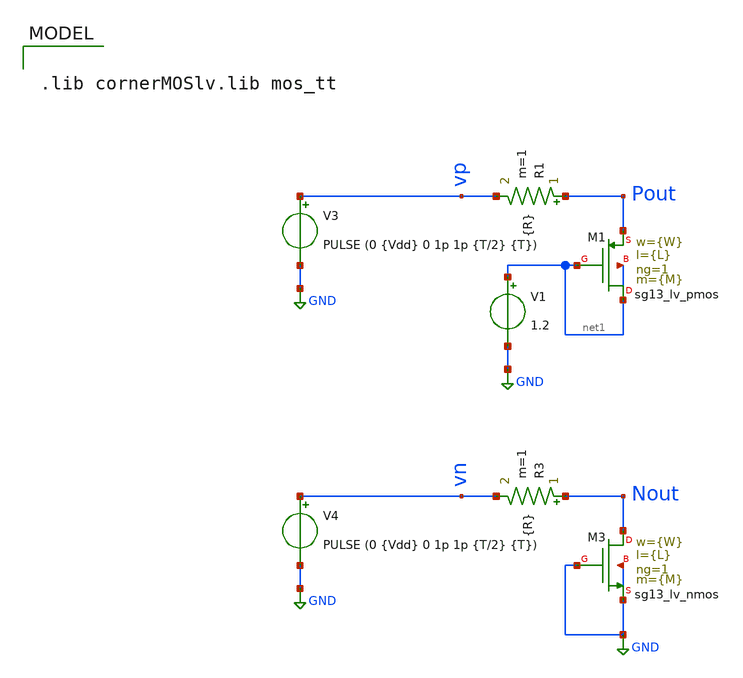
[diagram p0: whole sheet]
** sch_path: xschem/TB/TB_lvmos_Cdrain.sch
**.subckt TB_lvmos_Cdrain
R1 Pout vp {R} m=1
V3 vp GND PULSE (0 {Vdd} 0 1p 1p {T/2} {T})
V1 net1 GND 1.2
R3 Nout vn {R} m=1
V4 vn GND PULSE (0 {Vdd} 0 1p 1p {T/2} {T})
XM3 Nout GND GND GND sg13_lv_nmos w={W} l={L} ng=1 m={M} mm_ok=1
XM1 net1 net1 Pout net1 sg13_lv_pmos w={W} l={L} ng=1 m={M} mm_ok=1
**** begin user architecture code

.lib cornerMOSlv.lib mos_tt



.param R = 100k
.parameter T = 10n
.param Vdd = 1.8

.ic v(Pout) = 0
.ic v(Nout) = 0

* MOS Param
.param temp=27
.param M = 1
.param W = 1u
.param L = 0.2u




.control
let strt_w = 0.25u
let stop_w = 10u
let step_w = 0.1u
let curr_w = 1.0u
save all
while curr_w le stop_w
	alterparam W = $&curr_w
	reset
	tran 10p 2n
	meas tran tauN when v(Nout) = 1.138 CROSS=1
	meas tran tauP when v(Pout) = 1.138 CROSS=1
	let Cn = tauN/(100k)
	let Cp = tauP/(100k)
	wrdata ../proyecto-IPD413/simulations/Cap_vs_Width.raw Cn Cp curr_w
	set appendwrite
	let curr_w = curr_w + step_w
end
plot v(Nout)
.endc


**** end user architecture code
**.ends
.GLOBAL GND
.end
